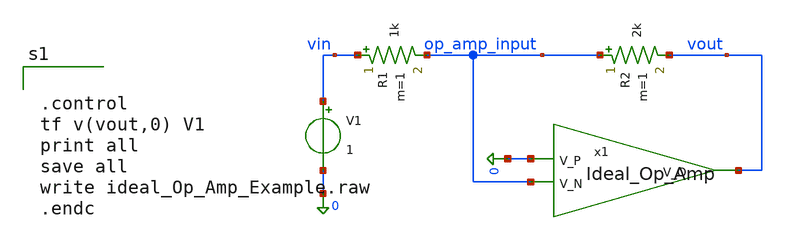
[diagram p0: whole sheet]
** sch_path: mag/layout/Ideal_Op_Amp_Example.sch
**.subckt Ideal_Op_Amp_Example
R1 vin op_amp_input 1k m=1
R2 op_amp_input vout 2k m=1
V1 vin 0 1
x1 vout 0 op_amp_input Ideal_Op_Amp
**** begin user architecture code


.control
tf v(vout,0) V1
print all
save all
write ideal_Op_Amp_Example.raw
.endc

**** end user architecture code
**.ends
.end
